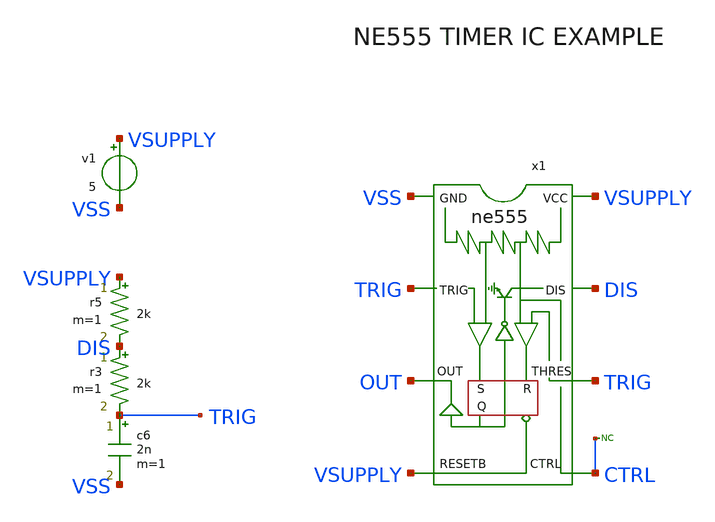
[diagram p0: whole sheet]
** sch_path: xschem-src/xschem_library/examples/test_ne555.sch
* Copyright (C) 1998-2026 Stefan Frederik Schippers
* This program is free software; you can redistribute it and/or modify
* it under the terms of the GNU General Public License as published by
* the Free Software Foundation; either version 2 of the License, or
* (at your option) any later version.
* This program is distributed in the hope that it will be useful,
* but WITHOUT ANY WARRANTY; without even the implied warranty of
* MERCHANTABILITY or FITNESS FOR A PARTICULAR PURPOSE.  See the
* GNU General Public License for more details.
* You should have received a copy of the GNU General Public License
* along with this program; if not, write to the Free Software
**.subckt test_ne555
x1 VSS TRIG OUT VSUPPLY CTRL TRIG DIS VSUPPLY ne555
r3 DIS TRIG 2k m=1
c6 TRIG VSS 2n m=1
v1 VSUPPLY VSS 5
r5 VSUPPLY DIS 2k m=1
* noconn CTRL
**** begin user architecture code

.option SCALE=1e-6 PARHIER=LOCAL RUNLVL=6 post MODMONTE=1
.option sampling_method = SRS
* .option method=gear
vvss vss 0 dc 0

** models are generally not free: you must download
** SPICE models for active devices and put them  into the below
** referenced file in netlist/simulation directory.
.temp 30
* .include "model_test_ne555.txt"

.control
  save all
  tran 0.1u 1m uic
  write test_ne555.raw
.endc


**** end user architecture code
**.ends

* expanding   symbol:  ne555.sym # of pins=8
** sym_path: xschem-src/xschem_library/examples/ne555.sym
.include $netlist_dir/model_test_ne555.txt
.end
